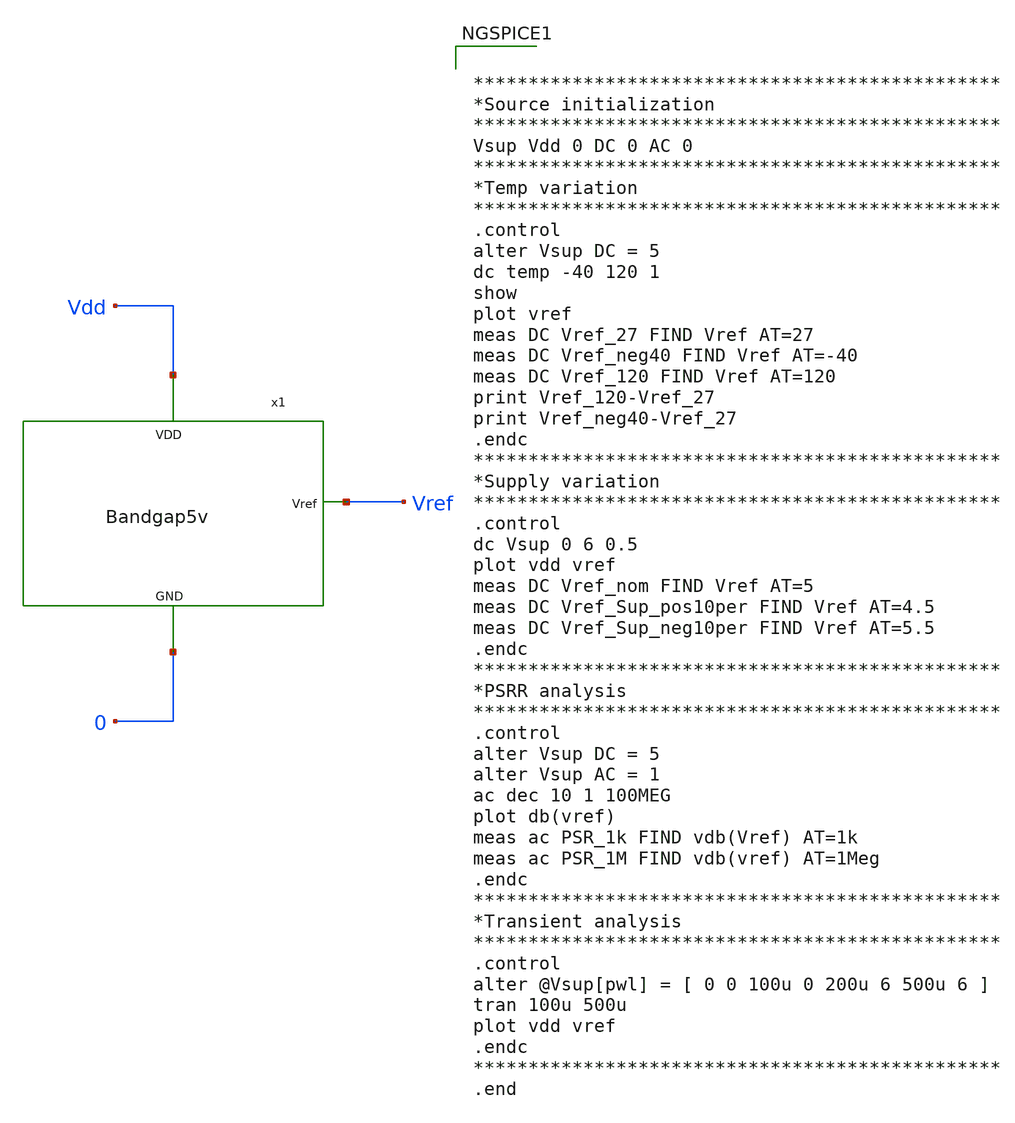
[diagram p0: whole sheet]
** sch_path: Analog_blocks/Analog_Blocks/Bandgap/Testbench/Bandgap5v_meas.sch
**.subckt Bandgap5v_meas
x1 Vref Vdd 0 Bandgap5v
**** begin user architecture code

.include ~/Analog_blocks/models/skywater-pdk/libraries/sky130_fd_pr/latest/cells/nfet_01v8/sky130_fd_pr__nfet_01v8__tt.corner.spice
.include ~/Analog_blocks/models/skywater-pdk/libraries/sky130_fd_pr/latest/cells/nfet_01v8_lvt/sky130_fd_pr__nfet_01v8_lvt__tt.corner.spice
.include ~/Analog_blocks/models/skywater-pdk/libraries/sky130_fd_pr/latest/cells/pfet_01v8/sky130_fd_pr__pfet_01v8__tt.corner.spice
.include ~/Analog_blocks/models/skywater-pdk/libraries/sky130_fd_pr/latest/cells/nfet_03v3_nvt/sky130_fd_pr__nfet_03v3_nvt__tt.corner.spice
.include ~/Analog_blocks/models/skywater-pdk/libraries/sky130_fd_pr/latest/cells/nfet_05v0_nvt/sky130_fd_pr__nfet_05v0_nvt__tt.corner.spice
.include ~/Analog_blocks/models/skywater-pdk/libraries/sky130_fd_pr/latest/cells/esd_nfet_01v8/sky130_fd_pr__esd_nfet_01v8__tt.corner.spice
.include ~/Analog_blocks/models/skywater-pdk/libraries/sky130_fd_pr/latest/cells/pfet_01v8_lvt/sky130_fd_pr__pfet_01v8_lvt__tt.corner.spice
.include ~/Analog_blocks/models/skywater-pdk/libraries/sky130_fd_pr/latest/cells/pfet_01v8_hvt/sky130_fd_pr__pfet_01v8_hvt__tt.corner.spice
.include ~/Analog_blocks/models/skywater-pdk/libraries/sky130_fd_pr/latest/cells/esd_pfet_g5v0d10v5/sky130_fd_pr__esd_pfet_g5v0d10v5__tt.corner.spice
.include ~/Analog_blocks/models/skywater-pdk/libraries/sky130_fd_pr/latest/cells/pfet_g5v0d10v5/sky130_fd_pr__pfet_g5v0d10v5__tt.corner.spice
.include ~/Analog_blocks/models/skywater-pdk/libraries/sky130_fd_pr/latest/cells/pfet_g5v0d16v0/sky130_fd_pr__pfet_g5v0d16v0__tt.corner.spice
.include ~/Analog_blocks/models/skywater-pdk/libraries/sky130_fd_pr/latest/cells/nfet_g5v0d10v5/sky130_fd_pr__nfet_g5v0d10v5__tt.corner.spice
.include ~/Analog_blocks/models/skywater-pdk/libraries/sky130_fd_pr/latest/cells/nfet_g5v0d16v0/sky130_fd_pr__nfet_g5v0d16v0__tt_discrete.corner.spice
.include ~/Analog_blocks/models/skywater-pdk/libraries/sky130_fd_pr/latest/cells/esd_nfet_g5v0d10v5/sky130_fd_pr__esd_nfet_g5v0d10v5__tt.corner.spice
.include ~/Analog_blocks/models/skywater-pdk/libraries/sky130_fd_pr/latest/models/corners/tt/nonfet.spice
* Mismatch parameters
.include ~/Analog_blocks/models/skywater-pdk/libraries/sky130_fd_pr/latest/cells/nfet_01v8/sky130_fd_pr__nfet_01v8__mismatch.corner.spice
.include ~/Analog_blocks/models/skywater-pdk/libraries/sky130_fd_pr/latest/cells/pfet_01v8/sky130_fd_pr__pfet_01v8__mismatch.corner.spice
.include ~/Analog_blocks/models/skywater-pdk/libraries/sky130_fd_pr/latest/cells/nfet_01v8_lvt/sky130_fd_pr__nfet_01v8_lvt__mismatch.corner.spice
.include ~/Analog_blocks/models/skywater-pdk/libraries/sky130_fd_pr/latest/cells/pfet_01v8_lvt/sky130_fd_pr__pfet_01v8_lvt__mismatch.corner.spice
.include ~/Analog_blocks/models/skywater-pdk/libraries/sky130_fd_pr/latest/cells/pfet_01v8_hvt/sky130_fd_pr__pfet_01v8_hvt__mismatch.corner.spice
.include ~/Analog_blocks/models/skywater-pdk/libraries/sky130_fd_pr/latest/cells/nfet_g5v0d10v5/sky130_fd_pr__nfet_g5v0d10v5__mismatch.corner.spice
.include ~/Analog_blocks/models/skywater-pdk/libraries/sky130_fd_pr/latest/cells/pfet_g5v0d10v5/sky130_fd_pr__pfet_g5v0d10v5__mismatch.corner.spice
.include ~/Analog_blocks/models/skywater-pdk/libraries/sky130_fd_pr/latest/cells/nfet_05v0_nvt/sky130_fd_pr__nfet_05v0_nvt__mismatch.corner.spice
.include ~/Analog_blocks/models/skywater-pdk/libraries/sky130_fd_pr/latest/cells/nfet_03v3_nvt/sky130_fd_pr__nfet_03v3_nvt__mismatch.corner.spice
* Resistor
.include ~/Analog_blocks/models/skywater-pdk/libraries/sky130_fd_pr/latest/models/r+c/res_typical__cap_typical.spice
.include ~/Analog_blocks/models/skywater-pdk/libraries/sky130_fd_pr/latest/models/r+c/res_typical__cap_typical__lin.spice
* Special cells
.include ~/Analog_blocks/models/skywater-pdk/libraries/sky130_fd_pr/latest/models/corners/tt/specialized_cells.spice
* All models
.include ~/Analog_blocks/models/skywater-pdk/libraries/sky130_fd_pr/latest/models/all.spice
* Corner
.include ~/Analog_blocks/models/skywater-pdk/libraries/sky130_fd_pr/latest/models/corners/tt/rf.spice



************************************************
*Source initialization
************************************************
Vsup Vdd 0 DC 0 AC 0
************************************************
*Temp variation
************************************************
.control
alter Vsup DC = 5
dc temp -40 120 1
show
plot vref
meas DC Vref_27 FIND Vref AT=27
meas DC Vref_neg40 FIND Vref AT=-40
meas DC Vref_120 FIND Vref AT=120
print Vref_120-Vref_27
print Vref_neg40-Vref_27
.endc
************************************************
*Supply variation
************************************************
.control
dc Vsup 0 6 0.5
plot vdd vref
meas DC Vref_nom FIND Vref AT=5
meas DC Vref_Sup_pos10per FIND Vref AT=4.5
meas DC Vref_Sup_neg10per FIND Vref AT=5.5
.endc
************************************************
*PSRR analysis
************************************************
.control
alter Vsup DC = 5
alter Vsup AC = 1
ac dec 10 1 100MEG
plot db(vref)
meas ac PSR_1k FIND vdb(Vref) AT=1k
meas ac PSR_1M FIND vdb(vref) AT=1Meg
.endc
************************************************
*Transient analysis
************************************************
.control
alter @Vsup[pwl] = [ 0 0 100u 0 200u 6 500u 6 ]
tran 100u 500u
plot vdd vref
.endc
************************************************
.end


**** end user architecture code
**.ends

* expanding   symbol:
*+  /home/eslam/Analog_blocks/Analog_Blocks/Bandgap/Schematics/BGR5v/Bandgap5v.sym # of pins=3
** sym_path: Analog_Blocks/Bandgap/Schematics/BGR5v/Bandgap5v.sym
** sch_path: Analog_Blocks/Bandgap/Schematics/BGR5v/Bandgap5v.sch
.subckt Bandgap5v Vref VDD GND
*.ipin VDD
*.ipin GND
*.opin Vref
XQ1 GND GND net3 sky130_fd_pr__pnp_05v5_W0p68L0p68 m=1
XQ2 GND GND net1 sky130_fd_pr__pnp_05v5_W0p68L0p68 m=1
XQ3 GND GND net1 sky130_fd_pr__pnp_05v5_W0p68L0p68 m=1
XQ4 GND GND net1 sky130_fd_pr__pnp_05v5_W0p68L0p68 m=1
XQ5 GND GND net1 sky130_fd_pr__pnp_05v5_W0p68L0p68 m=1
XQ6 GND GND net1 sky130_fd_pr__pnp_05v5_W0p68L0p68 m=1
XQ7 GND GND net1 sky130_fd_pr__pnp_05v5_W0p68L0p68 m=1
XQ8 GND GND net1 sky130_fd_pr__pnp_05v5_W0p68L0p68 m=1
XQ9 GND GND net1 sky130_fd_pr__pnp_05v5_W0p68L0p68 m=1
XM2 net4 net5 VDD VDD sky130_fd_pr__pfet_g5v0d10v5 L=1 W=10 nf=1 ad='int((nf+1)/2) * W/nf * 0.29' as='int((nf+2)/2) * W/nf * 0.29'
+ pd='2*int((nf+1)/2) * (W/nf + 0.29)' ps='2*int((nf+2)/2) * (W/nf + 0.29)' nrd='0.29 / W' nrs='0.29 / W'
+ sa=0 sb=0 sd=0 mult=1 m=1
XM3 net3 net4 VDD VDD sky130_fd_pr__pfet_g5v0d10v5 L=1 W=10 nf=1 ad='int((nf+1)/2) * W/nf * 0.29' as='int((nf+2)/2) * W/nf * 0.29'
+ pd='2*int((nf+1)/2) * (W/nf + 0.29)' ps='2*int((nf+2)/2) * (W/nf + 0.29)' nrd='0.29 / W' nrs='0.29 / W'
+ sa=0 sb=0 sd=0 mult=1 m=1
XM1 net4 net5 GND GND sky130_fd_pr__nfet_g5v0d10v5 L=40 W=1 nf=1 ad='int((nf+1)/2) * W/nf * 0.29' as='int((nf+2)/2) * W/nf * 0.29'
+ pd='2*int((nf+1)/2) * (W/nf + 0.29)' ps='2*int((nf+2)/2) * (W/nf + 0.29)' nrd='0.29 / W' nrs='0.29 / W'
+ sa=0 sb=0 sd=0 mult=1 m=1
XR1 net2 Vref GND sky130_fd_pr__res_high_po W=1 L=6 mult=1 m=1
XR3 net3 Vref GND sky130_fd_pr__res_high_po W=1 L=6 mult=1 m=1
XR2 net1 net2 GND sky130_fd_pr__res_high_po W=1 L=2.6 mult=1 m=1
x1 VDD net3 net2 Vref net5 GND Bandgap5v_OTA
.ends


* expanding   symbol:  /home/eslam/Analog_Design/LDO/Schematic/Bandgap5v_OTA.sym # of pins=6
** sym_path: LDO/Schematic/Bandgap5v_OTA.sym
** sch_path: LDO/Schematic/Bandgap5v_OTA.sch
.subckt Bandgap5v_OTA Vdd Vn Vp Ibias Vhigh Gnd
*.opin Ibias
*.ipin Vhigh
*.ipin Vdd
*.ipin Gnd
*.ipin Vn
*.ipin Vp
XM6 Ibias Vhigh Vdd Vdd sky130_fd_pr__pfet_g5v0d10v5 L=1 W=10 nf=1 ad='int((nf+1)/2) * W/nf * 0.29' as='int((nf+2)/2) * W/nf * 0.29'
+ pd='2*int((nf+1)/2) * (W/nf + 0.29)' ps='2*int((nf+2)/2) * (W/nf + 0.29)' nrd='0.29 / W' nrs='0.29 / W'
+ sa=0 sb=0 sd=0 mult=1 m=1
XM5 net3 Vhigh Vdd Vdd sky130_fd_pr__pfet_g5v0d10v5 L=1 W=10 nf=1 ad='int((nf+1)/2) * W/nf * 0.29' as='int((nf+2)/2) * W/nf * 0.29'
+ pd='2*int((nf+1)/2) * (W/nf + 0.29)' ps='2*int((nf+2)/2) * (W/nf + 0.29)' nrd='0.29 / W' nrs='0.29 / W'
+ sa=0 sb=0 sd=0 mult=1 m=1
XM7 Vhigh Vhigh Vdd Vdd sky130_fd_pr__pfet_g5v0d10v5 L=1 W=54 nf=1 ad='int((nf+1)/2) * W/nf * 0.29' as='int((nf+2)/2) * W/nf * 0.29'
+ pd='2*int((nf+1)/2) * (W/nf + 0.29)' ps='2*int((nf+2)/2) * (W/nf + 0.29)' nrd='0.29 / W' nrs='0.29 / W'
+ sa=0 sb=0 sd=0 mult=1 m=1
XM2 net1 Vp net3 Vdd sky130_fd_pr__pfet_g5v0d10v5 L=1 W=30 nf=1 ad='int((nf+1)/2) * W/nf * 0.29' as='int((nf+2)/2) * W/nf * 0.29'
+ pd='2*int((nf+1)/2) * (W/nf + 0.29)' ps='2*int((nf+2)/2) * (W/nf + 0.29)' nrd='0.29 / W' nrs='0.29 / W'
+ sa=0 sb=0 sd=0 mult=1 m=1
XM1 net2 Vn net3 Vdd sky130_fd_pr__pfet_g5v0d10v5 L=1 W=30 nf=1 ad='int((nf+1)/2) * W/nf * 0.29' as='int((nf+2)/2) * W/nf * 0.29'
+ pd='2*int((nf+1)/2) * (W/nf + 0.29)' ps='2*int((nf+2)/2) * (W/nf + 0.29)' nrd='0.29 / W' nrs='0.29 / W'
+ sa=0 sb=0 sd=0 mult=1 m=1
XM8 Vhigh net1 Gnd Gnd sky130_fd_pr__nfet_g5v0d10v5 L=0.5 W=75 nf=1 ad='int((nf+1)/2) * W/nf * 0.29'
+ as='int((nf+2)/2) * W/nf * 0.29' pd='2*int((nf+1)/2) * (W/nf + 0.29)' ps='2*int((nf+2)/2) * (W/nf + 0.29)'
+ nrd='0.29 / W' nrs='0.29 / W' sa=0 sb=0 sd=0 mult=1 m=1
XM4 net1 net2 Gnd Gnd sky130_fd_pr__nfet_g5v0d10v5 L=0.5 W=7.5 nf=1 ad='int((nf+1)/2) * W/nf * 0.29'
+ as='int((nf+2)/2) * W/nf * 0.29' pd='2*int((nf+1)/2) * (W/nf + 0.29)' ps='2*int((nf+2)/2) * (W/nf + 0.29)'
+ nrd='0.29 / W' nrs='0.29 / W' sa=0 sb=0 sd=0 mult=1 m=1
XM3 net2 net2 Gnd Gnd sky130_fd_pr__nfet_g5v0d10v5 L=0.5 W=7.5 nf=1 ad='int((nf+1)/2) * W/nf * 0.29'
+ as='int((nf+2)/2) * W/nf * 0.29' pd='2*int((nf+1)/2) * (W/nf + 0.29)' ps='2*int((nf+2)/2) * (W/nf + 0.29)'
+ nrd='0.29 / W' nrs='0.29 / W' sa=0 sb=0 sd=0 mult=1 m=1
XC1 net1 Vhigh sky130_fd_pr__cap_mim_m3_2 W=1 L=1 MF=1 m=1
.ends

.end
